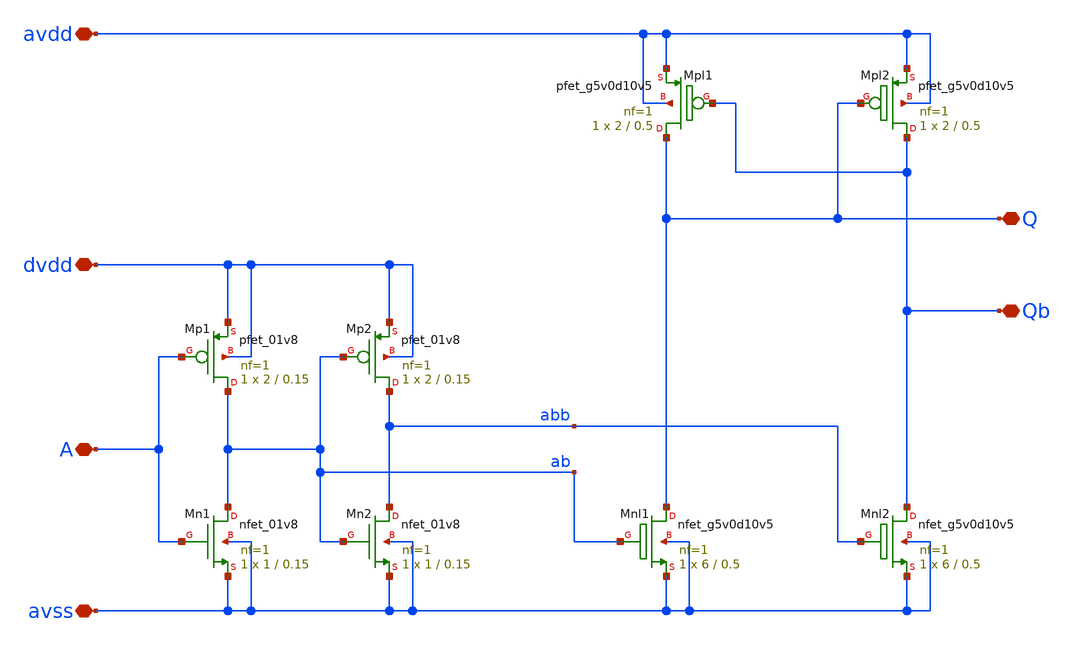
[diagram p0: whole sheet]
** sch_path: xschem/sky130_cm_levelshifter.sch
**.subckt sky130_cm_levelshifter avss avdd A dvdd Qb Q
*.iopin avss
*.iopin avdd
*.iopin A
*.iopin dvdd
*.iopin Qb
*.iopin Q
XMnl1 Q ab avss avss sky130_fd_pr__nfet_g5v0d10v5 L=0.5 W=6 nf=1 ad='int((1 + 1)/2) * 6 / 1 * 0.29' as='int((1 + 2)/2) * 6 / 1 * 0.29'
+ pd='2*int((1 + 1)/2) * (6 / 1 + 0.29)' ps='2*int((1 + 2)/2) * (6 / 1 + 0.29)' nrd='0.29 / 6 ' nrs='0.29 / 6 '
+ sa=0 sb=0 sd=0 mult=1 m=1
XMnl2 Qb abb avss avss sky130_fd_pr__nfet_g5v0d10v5 L=0.5 W=6 nf=1 ad='int((1 + 1)/2) * 6 / 1 * 0.29'
+ as='int((1 + 2)/2) * 6 / 1 * 0.29' pd='2*int((1 + 1)/2) * (6 / 1 + 0.29)' ps='2*int((1 + 2)/2) * (6 / 1 + 0.29)'
+ nrd='0.29 / 6 ' nrs='0.29 / 6 ' sa=0 sb=0 sd=0 mult=1 m=1
XMpl1 Q Qb avdd avdd sky130_fd_pr__pfet_g5v0d10v5 L=0.5 W=2 nf=1 ad='int((1 + 1)/2) * 2 / 1 * 0.29' as='int((1 + 2)/2) * 2 / 1 * 0.29'
+ pd='2*int((1 + 1)/2) * (2 / 1 + 0.29)' ps='2*int((1 + 2)/2) * (2 / 1 + 0.29)' nrd='0.29 / 2 ' nrs='0.29 / 2 '
+ sa=0 sb=0 sd=0 mult=1 m=1
XMpl2 Qb Q avdd avdd sky130_fd_pr__pfet_g5v0d10v5 L=0.5 W=2 nf=1 ad='int((1 + 1)/2) * 2 / 1 * 0.29' as='int((1 + 2)/2) * 2 / 1 * 0.29'
+ pd='2*int((1 + 1)/2) * (2 / 1 + 0.29)' ps='2*int((1 + 2)/2) * (2 / 1 + 0.29)' nrd='0.29 / 2 ' nrs='0.29 / 2 '
+ sa=0 sb=0 sd=0 mult=1 m=1
XMn1 ab A avss avss sky130_fd_pr__nfet_01v8 L=0.15 W=1 nf=1 ad='int((1 + 1)/2) * 1 / 1 * 0.29' as='int((1 + 2)/2) * 1 / 1 * 0.29'
+ pd='2*int((1 + 1)/2) * (1 / 1 + 0.29)' ps='2*int((1 + 2)/2) * (1 / 1 + 0.29)' nrd='0.29 / 1 ' nrs='0.29 / 1 '
+ sa=0 sb=0 sd=0 mult=1 m=1
XMp1 ab A dvdd dvdd sky130_fd_pr__pfet_01v8 L=0.15 W=2 nf=1 ad='int((nf+1)/2) * W/nf * 0.29' as='int((nf+2)/2) * W/nf * 0.29'
+ pd='2*int((nf+1)/2) * (W/nf + 0.29)' ps='2*int((nf+2)/2) * (W/nf + 0.29)' nrd='0.29 / W' nrs='0.29 / W'
+ sa=0 sb=0 sd=0 mult=1 m=1
XMn2 abb ab avss avss sky130_fd_pr__nfet_01v8 L=0.15 W=1 nf=1 ad='int((1 + 1)/2) * 1 / 1 * 0.29' as='int((1 + 2)/2) * 1 / 1 * 0.29'
+ pd='2*int((1 + 1)/2) * (1 / 1 + 0.29)' ps='2*int((1 + 2)/2) * (1 / 1 + 0.29)' nrd='0.29 / 1 ' nrs='0.29 / 1 '
+ sa=0 sb=0 sd=0 mult=1 m=1
XMp2 abb ab dvdd dvdd sky130_fd_pr__pfet_01v8 L=0.15 W=2 nf=1 ad='int((nf+1)/2) * W/nf * 0.29' as='int((nf+2)/2) * W/nf * 0.29'
+ pd='2*int((nf+1)/2) * (W/nf + 0.29)' ps='2*int((nf+2)/2) * (W/nf + 0.29)' nrd='0.29 / W' nrs='0.29 / W'
+ sa=0 sb=0 sd=0 mult=1 m=1
**.ends
.end
